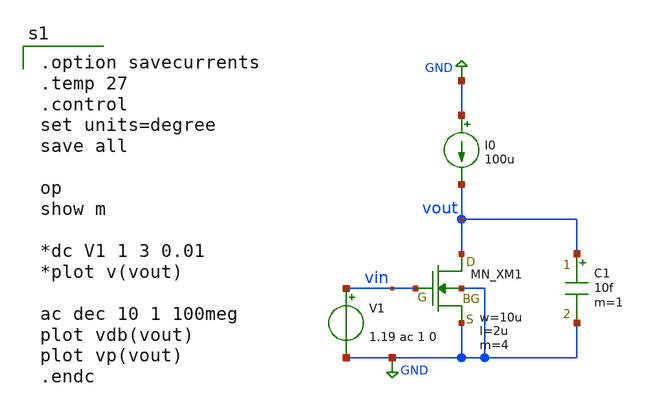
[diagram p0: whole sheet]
** sch_path: TR10/2026_AM-Radio/test_mos_ft/test_mos_ft.sch
**.subckt test_mos_ft
XM1 vout vin GND GND NMOS w=10u l=2u as=0 ad=0 ps=0 pd=0 nrd=0 nrs=0 m=4
V1 vin GND 1.19 ac 1 0
I0 GND vout 100u
C1 vout GND 10f m=1
**** begin user architecture code
 .include $::LIB/../ip62_models

.option savecurrents
.temp 27
.control
set units=degree
save all

op
show m

*dc V1 1 3 0.01
*plot v(vout)

ac dec 10 1 100meg
plot vdb(vout)
plot vp(vout)
.endc

**** end user architecture code
**.ends
.GLOBAL GND
.end
